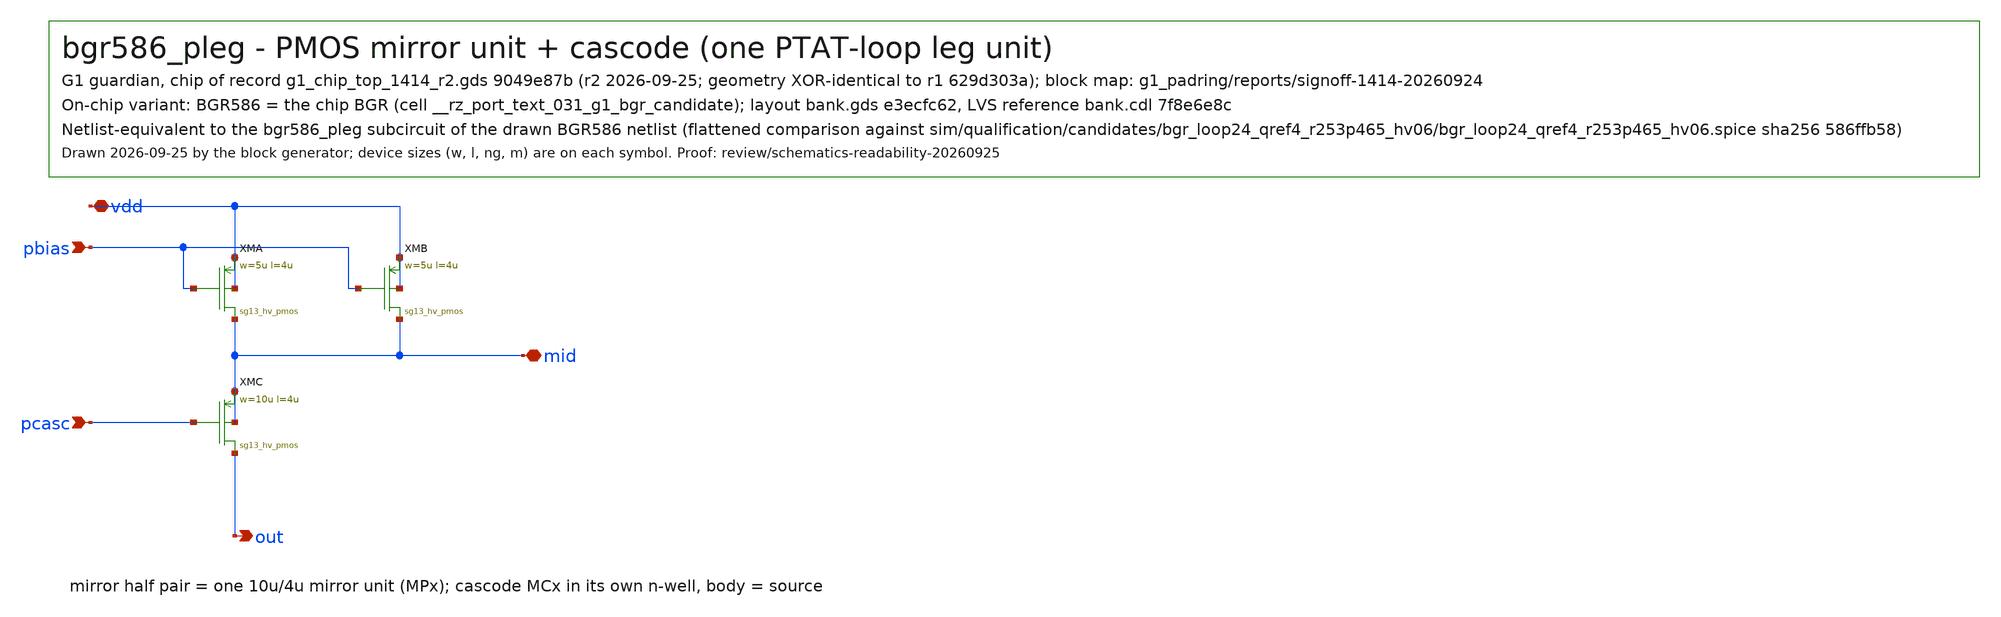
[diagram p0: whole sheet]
** sch_path: designs/g1-guardian/blocks/g1_bgr/xschem/bgr586/bgr586_pleg.sch
**.subckt bgr586_pleg out mid pbias pcasc vdd
*.opin out
*.iopin mid
*.ipin pbias
*.ipin pcasc
*.iopin vdd
XMA mid pbias vdd vdd sg13_hv_pmos l=4u w=5u as=1.7p ad=1.7p ps=10.68u pd=10.68u rfmode=0
XMB mid pbias vdd vdd sg13_hv_pmos l=4u w=5u as=1.7p ad=1.7p ps=10.68u pd=10.68u rfmode=0
XMC out pcasc mid mid sg13_hv_pmos l=4u w=10u as=3.4p ad=3.4p ps=20.68u pd=20.68u rfmode=0
**.ends
.end
